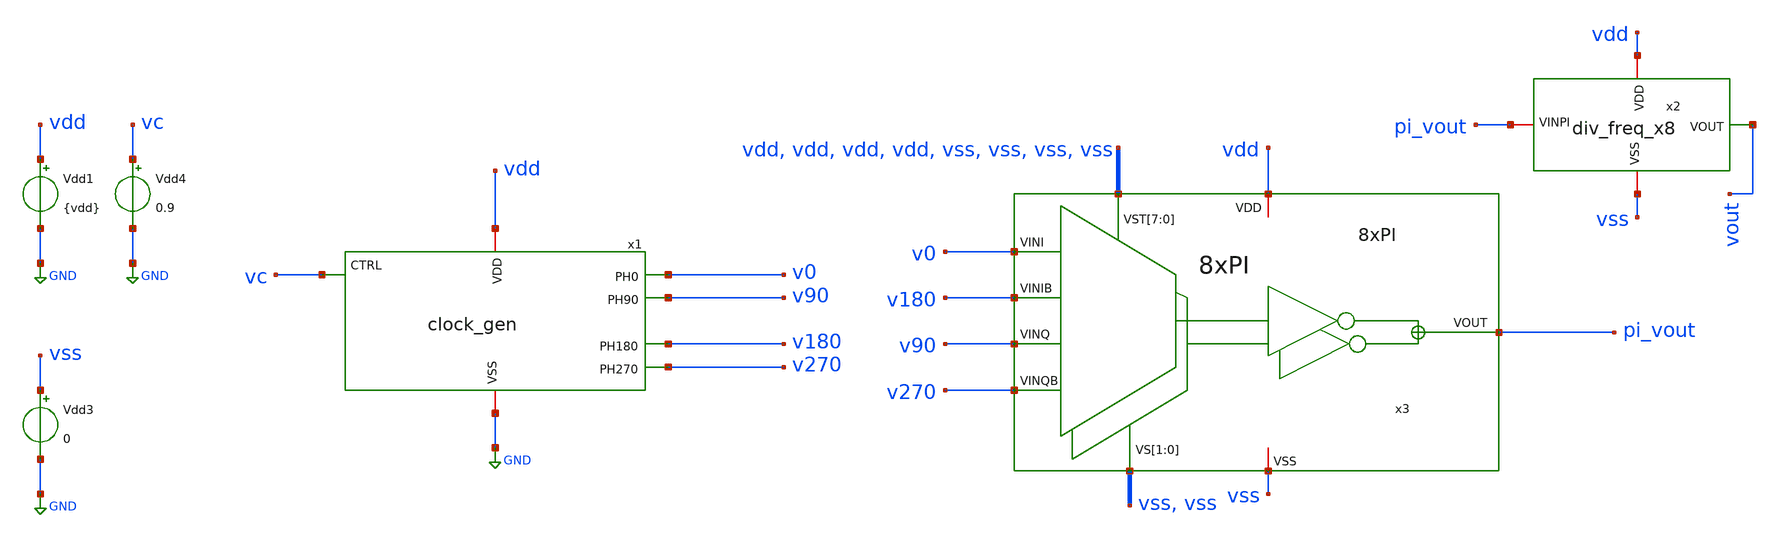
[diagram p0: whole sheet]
** sch_path: verification/testbenches/tb_2to4.sch
**.subckt tb_2to4
Vdd1 vdd GND {vdd}
Vdd4 vc GND 0.9
x3 v0 v180 v90 v270 vss vss vdd vdd vdd vdd vss vss vss vss pi_vout vdd vss 8xPI
Vdd3 vss GND 0
x1 v0 v90 vdd vc v180 GND v270 clock_gen
x2 vdd pi_vout vout vss div_freq_x8
**** begin user architecture code



.save v(vin1) v(v0) v(v90) v(v270) v(v180) v(vin2) v(vout) v(pi_vout) v(vdd)

.param vdd = 1.14
.options TEMP = -40

.tran 5p 16n
.save all

.control
run
set color0=white
write tran_logic.raw

meas tran ymax MAX v(vdd) from=0 to=1n
let vdd_half = ymax/2


*TT
*meas tran SKEW0_90 TRIG v(v0) VAL=vdd_half RISE=3 TARG v(v90) VAL=vdd_half RISE=4
*meas tran SKEW90_180 TRIG v(v90) VAL=vdd_half RISE=3 TARG v(v180) VAL=vdd_half RISE=3
*meas tran SKEW180_270 TRIG v(v180) VAL=vdd_half RISE=3 TARG v(v270) VAL=vdd_half RISE=4
*meas tran SKEW270_0 TRIG v(v270) VAL=vdd_half RISE=4 TARG v(v0) VAL=vdd_half RISE=3

*FF
*meas tran SKEW0_90 TRIG v(v0) VAL=vdd_half RISE=5 TARG v(v90) VAL=vdd_half RISE=5
*meas tran SKEW90_180 TRIG v(v90) VAL=vdd_half RISE=5 TARG v(v180) VAL=vdd_half RISE=6
*meas tran SKEW180_270 TRIG v(v180) VAL=vdd_half RISE=5 TARG v(v270) VAL=vdd_half RISE=5
*meas tran SKEW270_0 TRIG v(v270) VAL=vdd_half RISE=5 TARG v(v0) VAL=vdd_half RISE=5

*SS
meas tran SKEW0_90 TRIG v(v0) VAL=vdd_half RISE=15 TARG v(v90) VAL=vdd_half RISE=16
meas tran SKEW90_180 TRIG v(v90) VAL=vdd_half RISE=15 TARG v(v180) VAL=vdd_half RISE=16
meas tran SKEW180_270 TRIG v(v180) VAL=vdd_half RISE=15 TARG v(v270) VAL=vdd_half RISE=15
meas tran SKEW270_0 TRIG v(v270) VAL=vdd_half RISE=15 TARG v(v0) VAL=vdd_half RISE=15

meas tran T90 TRIG v(v90) VAL=vdd_half RISE=3 TARG v(v90) VAL=vdd_half RISE=4
meas tran T180 TRIG v(v180) VAL=vdd_half RISE=3 TARG v(v180) VAL=vdd_half RISE=4
meas tran T270 TRIG v(v270) VAL=vdd_half RISE=3 TARG v(v270) VAL=vdd_half RISE=4
meas tran T0 TRIG v(v0) VAL=vdd_half RISE=3 TARG v(v0) VAL=vdd_half RISE=4

let period_0 = T0
let period_90 = T90
let period_180 = T180
let period_270 = T270

let phase0_90 = (SKEW0_90 / period_0) * 360
let phase90_180 = (SKEW90_180 / period_0) * 360
let phase180_270 = (SKEW180_270 / period_0) * 360
let phase270_0 = (SKEW270_0 / period_0) * 360


meas tran PW0 TRIG v(v0) VAL=vdd_half RISE=3 TARG v(v0) VAL=vdd_half FALL=4
meas tran PW90 TRIG v(v90) VAL=vdd_half RISE=3 TARG v(v90) VAL=vdd_half FALL=4
meas tran PW180 TRIG v(v180) VAL=vdd_half RISE=3 TARG v(v180) VAL=vdd_half FALL=3
meas tran PW270 TRIG v(v270) VAL=vdd_half RISE=3 TARG v(v270) VAL=vdd_half FALL=3

let Duty0 = PW0 / period_0
let Duty90 = PW90 / period_90
let Duty180 = PW180 / period_180
let Duty270 = PW270 / period_270


let freq = 1 / period_0

print SKEW0_90 SKEW90_180 SKEW180_270 SKEW270_0 phase0_90 phase90_180 phase180_270 phase270_0 PW0
+ PW90 PW180 PW270 Duty0 Duty90 Duty180 Duty270 freq

.endc



.lib cornerMOSlv.lib mos_ss
*.include /foss/pdks/ihp-sg13g2/libs.ref/sg13g2_stdcell/spice/sg13g2_stdcell.spice


**** end user architecture code
**.ends
.GLOBAL GND
.end
